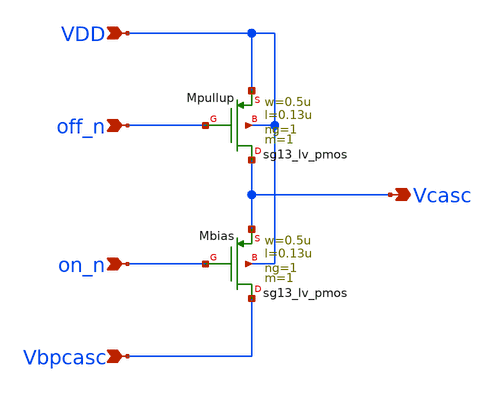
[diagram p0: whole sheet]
** sch_path: xschem/cascodeswitch_pmos.sch
**.subckt cascodeswitch_pmos off_n Vbpcasc Vcasc on_n VDD
*.ipin off_n
*.ipin Vbpcasc
*.opin Vcasc
*.ipin on_n
*.ipin VDD
XMpullup Vcasc off_n VDD VDD sg13_lv_pmos w=0.5u l=0.13u ng=1 m=1 mm_ok=1
XMbias Vbpcasc on_n Vcasc VDD sg13_lv_pmos w=0.5u l=0.13u ng=1 m=1 mm_ok=1
**.ends
.end
